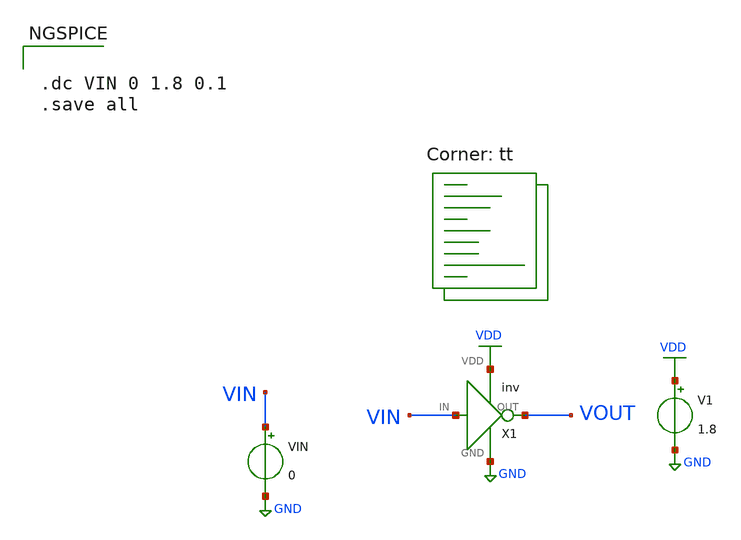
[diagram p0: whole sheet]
** sch_path: xschem/inv_tb.sch
**.subckt inv_tb
X1 VIN VOUT VDD GND inv
V1 VDD GND 1.8
VIN VIN GND 0
**** begin user architecture code
.lib $::SKYWATER_MODELS/sky130.lib.spice tt


.dc VIN 0 1.8 0.1
.save all


**** end user architecture code
**.ends

* expanding   symbol:  inv.sym # of pins=4
** sym_path: xschem/inv.sym
** sch_path: xschem/inv.sch
.subckt inv IN OUT VDD GND
*.ipin IN
*.opin OUT
*.iopin VDD
*.iopin GND
XM1 OUT IN GND GND sky130_fd_pr__nfet_01v8 L=0.15 W=1.5 nf=1 ad='int((nf+1)/2) * W/nf * 0.29' as='int((nf+2)/2) * W/nf * 0.29'
+ pd='2*int((nf+1)/2) * (W/nf + 0.29)' ps='2*int((nf+2)/2) * (W/nf + 0.29)' nrd='0.29 / W' nrs='0.29 / W'
+ sa=0 sb=0 sd=0 mult=1 m=1
XM2 OUT IN VDD VDD sky130_fd_pr__pfet_01v8 L=0.15 W=3 nf=1 ad='int((nf+1)/2) * W/nf * 0.29' as='int((nf+2)/2) * W/nf * 0.29'
+ pd='2*int((nf+1)/2) * (W/nf + 0.29)' ps='2*int((nf+2)/2) * (W/nf + 0.29)' nrd='0.29 / W' nrs='0.29 / W'
+ sa=0 sb=0 sd=0 mult=1 m=1
.ends

.GLOBAL VDD
.GLOBAL GND
.end
